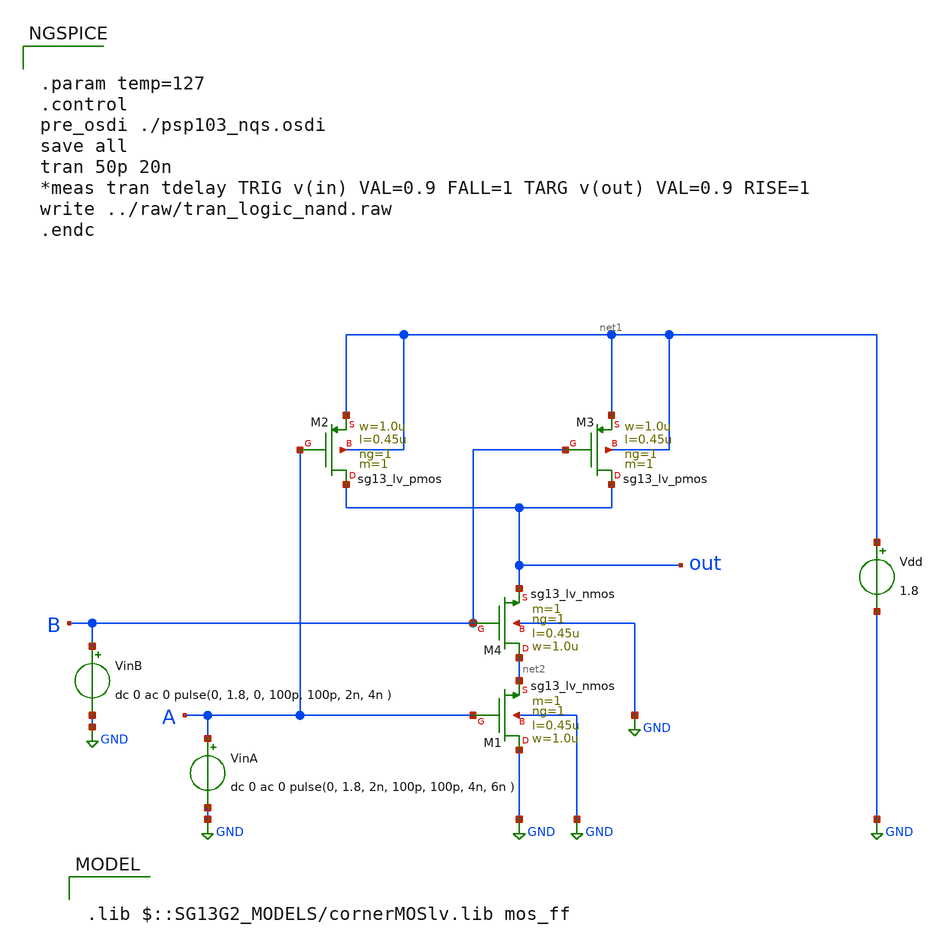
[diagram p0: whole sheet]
** sch_path: ihp-sg13g2/libs.tech/xschem/sg13g2_tests/tran_logic_nand.sch
* Copyright 2023 IHP PDK Authors
**.subckt tran_logic_nand
VinA A GND dc 0 ac 0 pulse(0, 1.8, 2n, 100p, 100p, 4n, 6n )
Vdd net1 GND 1.8
XM1 GND A net2 GND sg13_lv_nmos w=1.0u l=0.45u ng=1 m=1 mm_ok=1
XM2 out A net1 net1 sg13_lv_pmos w=1.0u l=0.45u ng=1 m=1 mm_ok=1
XM3 out B net1 net1 sg13_lv_pmos w=1.0u l=0.45u ng=1 m=1 mm_ok=1
XM4 net2 B out GND sg13_lv_nmos w=1.0u l=0.45u ng=1 m=1 mm_ok=1
VinB B GND dc 0 ac 0 pulse(0, 1.8, 0, 100p, 100p, 2n, 4n )
**** begin user architecture code

.lib $::SG13G2_MODELS/cornerMOSlv.lib mos_ff



.param temp=127
.control
pre_osdi ./psp103_nqs.osdi
save all
tran 50p 20n
*meas tran tdelay TRIG v(in) VAL=0.9 FALL=1 TARG v(out) VAL=0.9 RISE=1
write ../raw/tran_logic_nand.raw
.endc


**** end user architecture code
**.ends
.GLOBAL GND
.end
